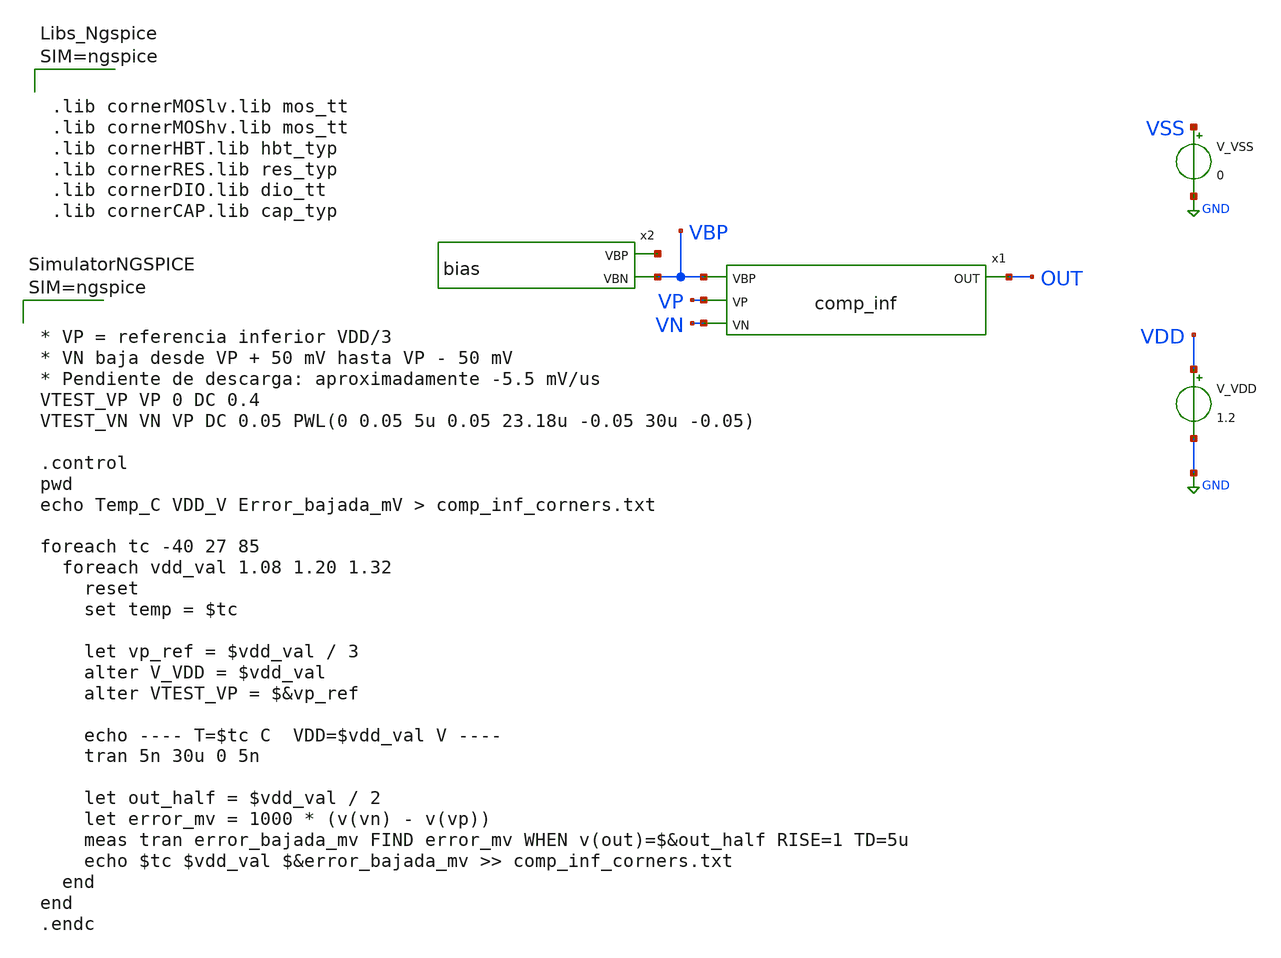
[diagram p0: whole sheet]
** sch_path: design/blocks/comparator/schematic/comp_inf_tb.sch
**.subckt comp_inf_tb
x2 net1 VBP VDD VSS bias
V_VDD VDD GND 1.2
V_VSS VSS GND 0
x1 VBP VP VN OUT VDD VSS comp_inf
**** begin user architecture code



.lib cornerMOSlv.lib mos_tt
.lib cornerMOShv.lib mos_tt
.lib cornerHBT.lib hbt_typ
.lib cornerRES.lib res_typ
.lib cornerDIO.lib dio_tt
.lib cornerCAP.lib cap_typ






* VP = referencia inferior VDD/3
* VN baja desde VP + 50 mV hasta VP - 50 mV
* Pendiente de descarga: aproximadamente -5.5 mV/us
VTEST_VP VP 0 DC 0.4
VTEST_VN VN VP DC 0.05 PWL(0 0.05 5u 0.05 23.18u -0.05 30u -0.05)

.control
pwd
echo Temp_C VDD_V Error_bajada_mV > comp_inf_corners.txt

foreach tc -40 27 85
  foreach vdd_val 1.08 1.20 1.32
    reset
    set temp = $tc

    let vp_ref = $vdd_val / 3
    alter V_VDD = $vdd_val
    alter VTEST_VP = $&vp_ref

    echo ---- T=$tc C  VDD=$vdd_val V ----
    tran 5n 30u 0 5n

    let out_half = $vdd_val / 2
    let error_mv = 1000 * (v(vn) - v(vp))
    meas tran error_bajada_mv FIND error_mv WHEN v(out)=$&out_half RISE=1 TD=5u
    echo $tc $vdd_val $&error_bajada_mv >> comp_inf_corners.txt
  end
end
.endc


**** end user architecture code
**.ends

* expanding   symbol:  bias.sym # of pins=2
** sym_path: design/blocks/bias/schematic/bias.sym
** sch_path: design/blocks/bias/schematic/bias.sch
.subckt bias VBP VBN VDD VSS
*.opin VBP
*.opin VBN
XM1 VBN VBN VSS VSS sg13_lv_nmos w=2u l=1u ng=1 m=1 mm_ok=1
XM2 VBP VBP VDD VDD sg13_lv_pmos w=2u l=1u ng=1 m=1 mm_ok=1
XR2 VBP VSS VSS rhigh w=0.5e-6 l=10.0e-6 m=1 b=0 mm_ok=1
XR1 VDD VBN VSS rhigh w=0.5e-6 l=10.0e-6 m=1 b=0 mm_ok=1
XC1 VBN VSS cap_cmim w=26.0e-6 l=26.0e-6 m=1 mm_ok=1
XC2 VDD VBP cap_cmim w=26.0e-6 l=26.0e-6 m=1 mm_ok=1
.ends


* expanding   symbol:  comp_inf.sym # of pins=4
** sym_path: design/blocks/comparator/schematic/comp_inf.sym
** sch_path: design/blocks/comparator/schematic/comp_inf.sch
.subckt comp_inf VBP VP VN OUT VDD VSS
*.opin OUT
*.ipin VN
*.ipin VP
*.ipin VBP
x1 net2 net1 VDD VSS sg13g2_inv_1
x2 OUT net2 VDD VSS sg13g2_inv_1
XM1 net3 VBP VDD VDD sg13_lv_pmos w=2u l=1u ng=1 m=1 mm_ok=1
XM7 net4 VP net3 VDD sg13_lv_pmos w=40u l=0.5u ng=5 m=1 mm_ok=1
XM8 net1 VN net3 VDD sg13_lv_pmos w=40u l=0.5u ng=5 m=1 mm_ok=1
XM9 net4 net4 VSS VSS sg13_lv_nmos w=4u l=1u ng=3 m=1 mm_ok=1
XM10 net1 net4 VSS VSS sg13_lv_nmos w=4u l=1u ng=3 m=1 mm_ok=1
.ends


* expanding   symbol:  sg13g2_inv_1.sym # of pins=2
** sym_path: sg13g2_inv_1.sym
** sch_path: sg13g2_inv_1.sch
.subckt sg13g2_inv_1 Y A VDD VSS
*.opin Y
*.ipin A
*.iopin VDD
*.iopin VSS
XM1 Y A VSS VSS sg13_lv_nmos w=740.00n l=130.00n ng=1 m=1 mm_ok=1
XM2 Y A VDD VDD sg13_lv_pmos w=1.12u l=130.00n ng=1 m=1 mm_ok=1
.ends

.GLOBAL GND
.end
